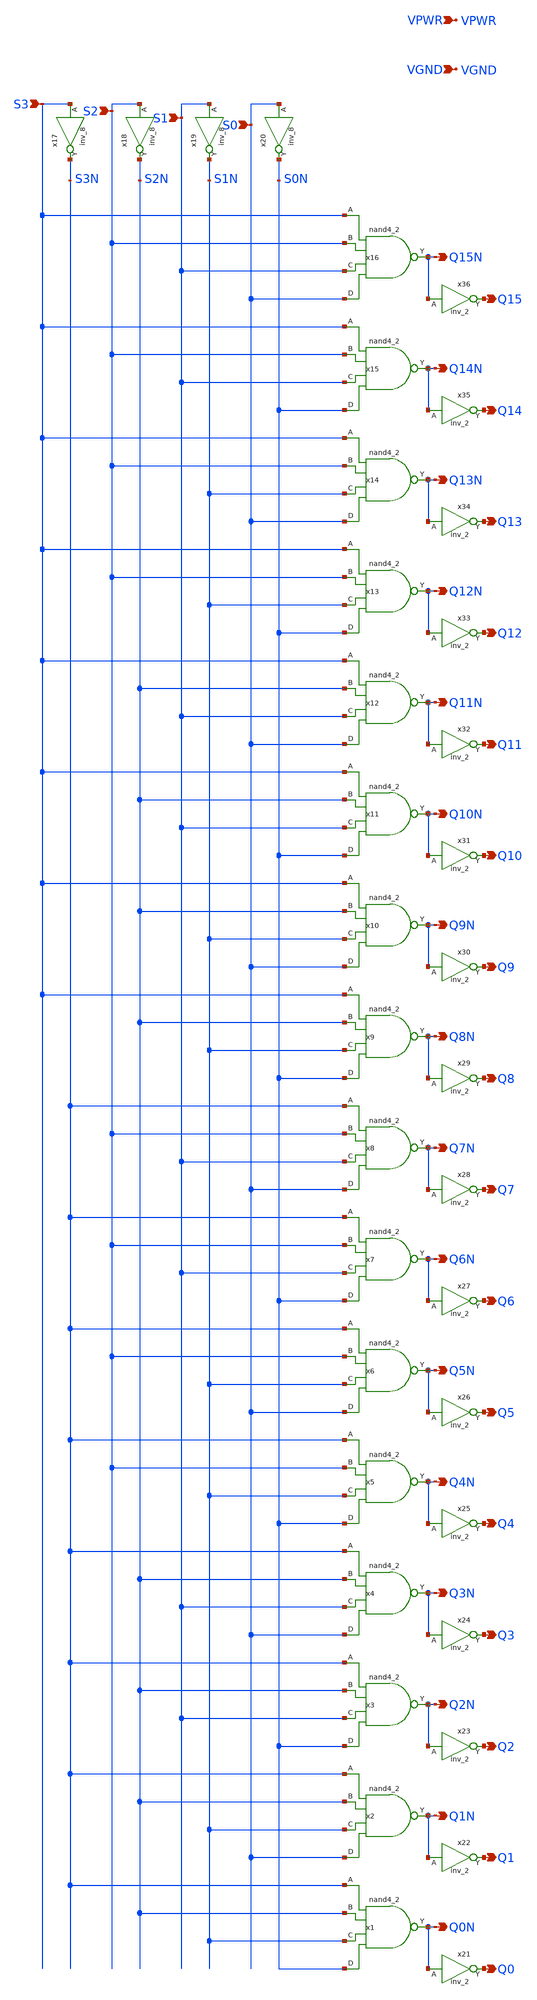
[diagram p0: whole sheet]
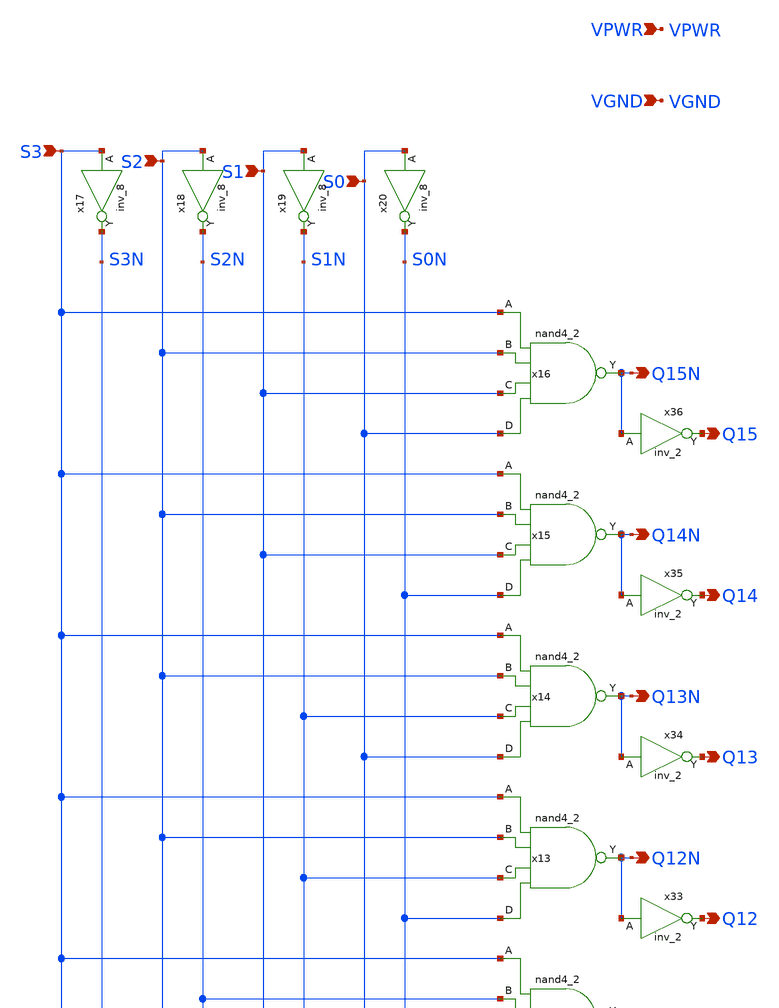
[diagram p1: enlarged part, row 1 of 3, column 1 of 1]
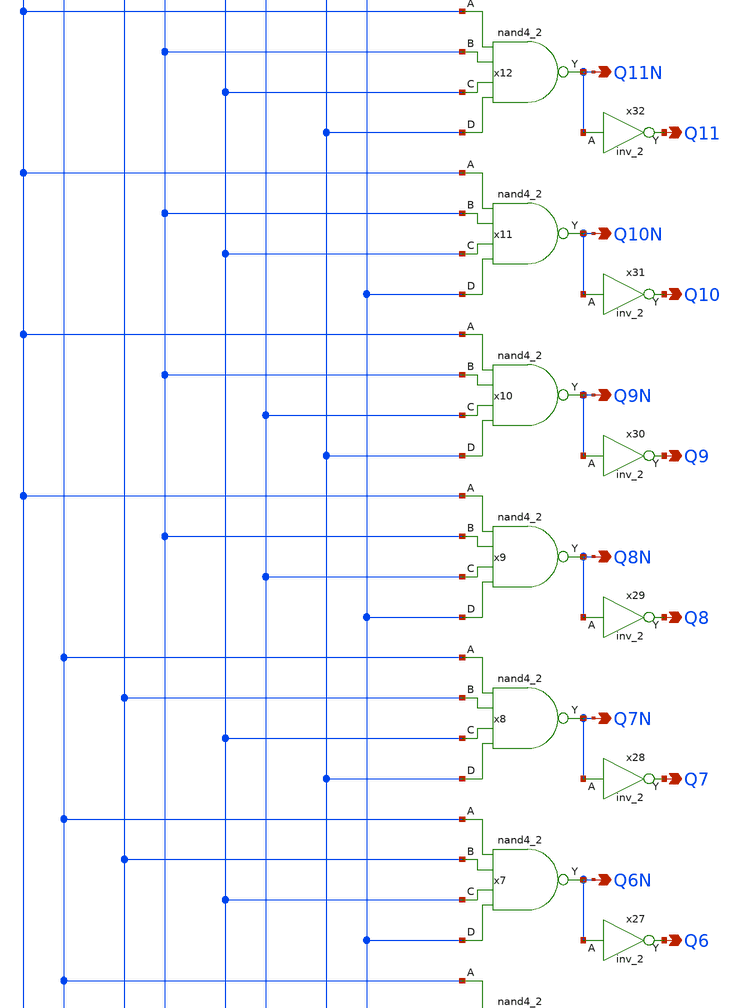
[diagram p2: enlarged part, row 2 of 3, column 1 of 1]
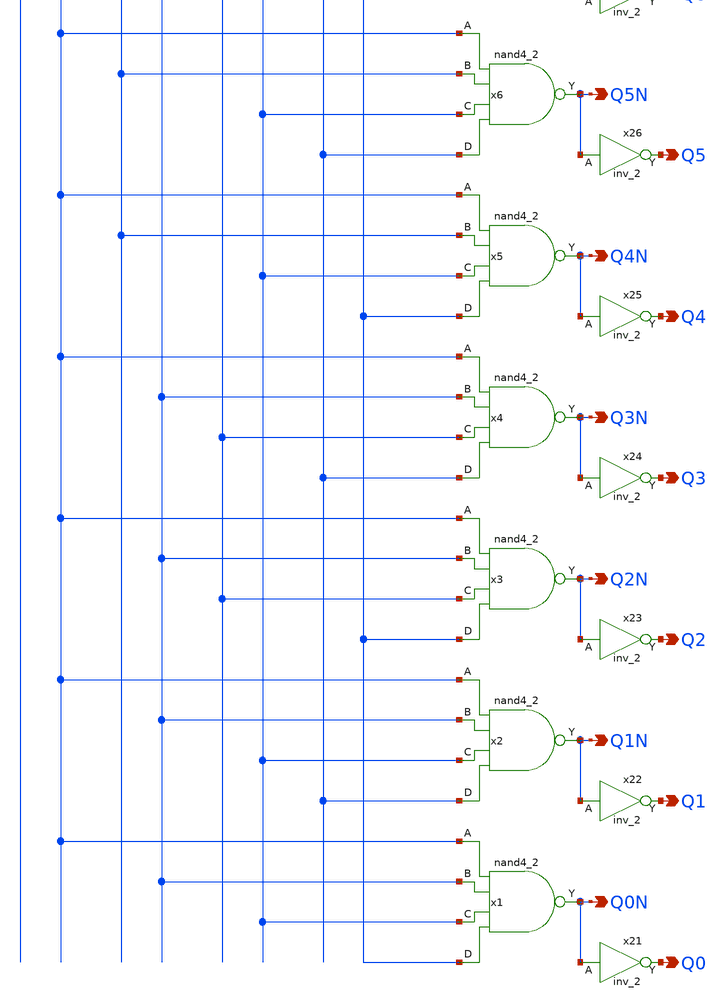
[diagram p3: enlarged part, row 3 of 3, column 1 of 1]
** sch_path: SP23_Tapeout/C2S2_Analog_TestChip-main/xschem/decoder_x4.sch

.include $::SKYWATER_STDCELLS/sky130_fd_sc_hd.spice

**.subckt decoder_x4 S3 S2 S1 S0 VGND VPWR Q14N Q15N Q13N Q12N Q10N Q11N Q9N Q8N Q7N Q6N Q4N Q3N Q2N
*+ Q1N Q0N Q5N Q14 Q15 Q13 Q12 Q10 Q11 Q9 Q8 Q7 Q6 Q4 Q3 Q2 Q1 Q0 Q5
*.ipin S3
*.ipin S2
*.ipin S1
*.ipin S0
*.ipin VGND
*.ipin VPWR
*.opin Q14N
*.opin Q15N
*.opin Q13N
*.opin Q12N
*.opin Q10N
*.opin Q11N
*.opin Q9N
*.opin Q8N
*.opin Q7N
*.opin Q6N
*.opin Q4N
*.opin Q3N
*.opin Q2N
*.opin Q1N
*.opin Q0N
*.opin Q5N
*.opin Q14
*.opin Q15
*.opin Q13
*.opin Q12
*.opin Q10
*.opin Q11
*.opin Q9
*.opin Q8
*.opin Q7
*.opin Q6
*.opin Q4
*.opin Q3
*.opin Q2
*.opin Q1
*.opin Q0
*.opin Q5
x17 S3 VGND VGND VPWR VPWR S3N sky130_fd_sc_hd__inv_8
x18 S2 VGND VGND VPWR VPWR S2N sky130_fd_sc_hd__inv_8
x19 S1 VGND VGND VPWR VPWR S1N sky130_fd_sc_hd__inv_8
x20 S0 VGND VGND VPWR VPWR S0N sky130_fd_sc_hd__inv_8
x21 Q0N VGND VGND VPWR VPWR Q0 sky130_fd_sc_hd__inv_2
x22 Q1N VGND VGND VPWR VPWR Q1 sky130_fd_sc_hd__inv_2
x23 Q2N VGND VGND VPWR VPWR Q2 sky130_fd_sc_hd__inv_2
x24 Q3N VGND VGND VPWR VPWR Q3 sky130_fd_sc_hd__inv_2
x1 S3N S2N S1N S0N VGND VGND VPWR VPWR Q0N sky130_fd_sc_hd__nand4_2
x2 S3N S2N S1N S0 VGND VGND VPWR VPWR Q1N sky130_fd_sc_hd__nand4_2
x3 S3N S2N S1 S0N VGND VGND VPWR VPWR Q2N sky130_fd_sc_hd__nand4_2
x4 S3N S2N S1 S0 VGND VGND VPWR VPWR Q3N sky130_fd_sc_hd__nand4_2
x5 S3N S2 S1N S0N VGND VGND VPWR VPWR Q4N sky130_fd_sc_hd__nand4_2
x6 S3N S2 S1N S0 VGND VGND VPWR VPWR Q5N sky130_fd_sc_hd__nand4_2
x7 S3N S2 S1 S0N VGND VGND VPWR VPWR Q6N sky130_fd_sc_hd__nand4_2
x8 S3N S2 S1 S0 VGND VGND VPWR VPWR Q7N sky130_fd_sc_hd__nand4_2
x9 S3 S2N S1N S0N VGND VGND VPWR VPWR Q8N sky130_fd_sc_hd__nand4_2
x10 S3 S2N S1N S0 VGND VGND VPWR VPWR Q9N sky130_fd_sc_hd__nand4_2
x11 S3 S2N S1 S0N VGND VGND VPWR VPWR Q10N sky130_fd_sc_hd__nand4_2
x12 S3 S2N S1 S0 VGND VGND VPWR VPWR Q11N sky130_fd_sc_hd__nand4_2
x13 S3 S2 S1N S0N VGND VGND VPWR VPWR Q12N sky130_fd_sc_hd__nand4_2
x14 S3 S2 S1N S0 VGND VGND VPWR VPWR Q13N sky130_fd_sc_hd__nand4_2
x15 S3 S2 S1 S0N VGND VGND VPWR VPWR Q14N sky130_fd_sc_hd__nand4_2
x16 S3 S2 S1 S0 VGND VGND VPWR VPWR Q15N sky130_fd_sc_hd__nand4_2
x25 Q4N VGND VGND VPWR VPWR Q4 sky130_fd_sc_hd__inv_2
x26 Q5N VGND VGND VPWR VPWR Q5 sky130_fd_sc_hd__inv_2
x27 Q6N VGND VGND VPWR VPWR Q6 sky130_fd_sc_hd__inv_2
x28 Q7N VGND VGND VPWR VPWR Q7 sky130_fd_sc_hd__inv_2
x29 Q8N VGND VGND VPWR VPWR Q8 sky130_fd_sc_hd__inv_2
x30 Q9N VGND VGND VPWR VPWR Q9 sky130_fd_sc_hd__inv_2
x31 Q10N VGND VGND VPWR VPWR Q10 sky130_fd_sc_hd__inv_2
x32 Q11N VGND VGND VPWR VPWR Q11 sky130_fd_sc_hd__inv_2
x33 Q12N VGND VGND VPWR VPWR Q12 sky130_fd_sc_hd__inv_2
x34 Q13N VGND VGND VPWR VPWR Q13 sky130_fd_sc_hd__inv_2
x35 Q14N VGND VGND VPWR VPWR Q14 sky130_fd_sc_hd__inv_2
x36 Q15N VGND VGND VPWR VPWR Q15 sky130_fd_sc_hd__inv_2
**.ends
.end
